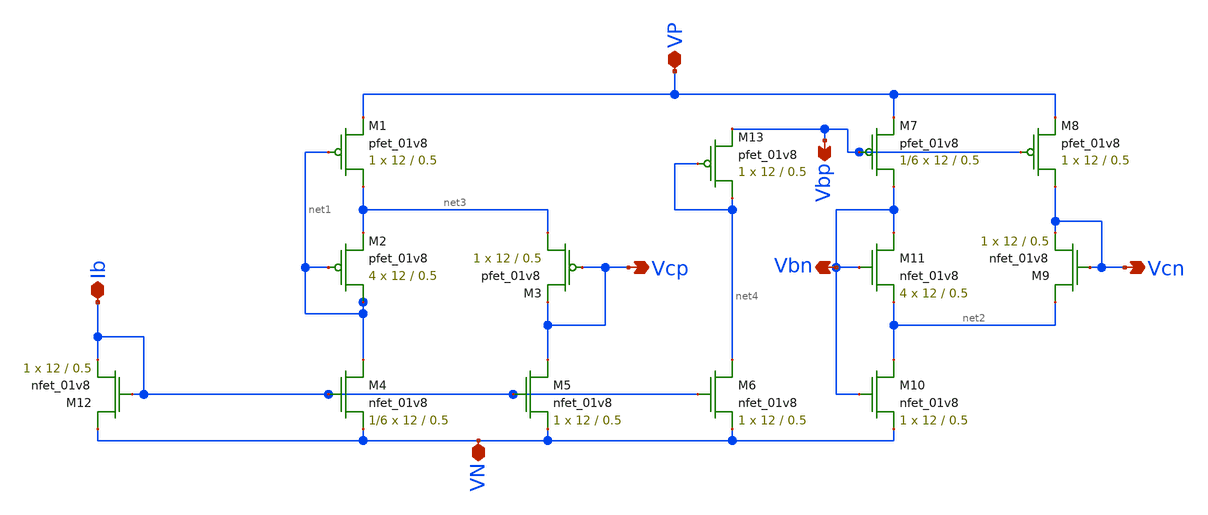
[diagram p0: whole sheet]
** sch_path: mp3/schematic/bias.sch
**.subckt bias VP VN Vcp Vcn Vbp Ib Vbn
*.iopin VP
*.iopin VN
*.opin Vcp
*.opin Vcn
*.opin Vbp
*.iopin Ib
*.opin Vbn
XM1 net3 net1 VP VDD sky130_fd_pr__pfet_01v8 L=0.5 W=12 nf=1 ad='int((nf+1)/2) * W/nf * 0.29' as='int((nf+2)/2) * W/nf * 0.29'
+ pd='2*int((nf+1)/2) * (W/nf + 0.29)' ps='2*int((nf+2)/2) * (W/nf + 0.29)' nrd='0.29 / W' nrs='0.29 / W'
+ sa=0 sb=0 sd=0 mult=1 m=1
XM2 net1 net1 net3 VDD sky130_fd_pr__pfet_01v8 L=0.5 W=12 nf=1 ad='int((nf+1)/2) * W/nf * 0.29' as='int((nf+2)/2) * W/nf * 0.29'
+ pd='2*int((nf+1)/2) * (W/nf + 0.29)' ps='2*int((nf+2)/2) * (W/nf + 0.29)' nrd='0.29 / W' nrs='0.29 / W'
+ sa=0 sb=0 sd=0 mult=4 m=4
XM3 net3 Vcp Vcp VDD sky130_fd_pr__pfet_01v8 L=0.5 W=12 nf=1 ad='int((nf+1)/2) * W/nf * 0.29' as='int((nf+2)/2) * W/nf * 0.29'
+ pd='2*int((nf+1)/2) * (W/nf + 0.29)' ps='2*int((nf+2)/2) * (W/nf + 0.29)' nrd='0.29 / W' nrs='0.29 / W'
+ sa=0 sb=0 sd=0 mult=1 m=1
XM4 net1 Ib VN GND sky130_fd_pr__nfet_01v8 L=0.5 W=12 nf=1 ad='int((nf+1)/2) * W/nf * 0.29' as='int((nf+2)/2) * W/nf * 0.29'
+ pd='2*int((nf+1)/2) * (W/nf + 0.29)' ps='2*int((nf+2)/2) * (W/nf + 0.29)' nrd='0.29 / W' nrs='0.29 / W'
+ sa=0 sb=0 sd=0 mult=1/6 m=1/6
XM5 Vcp Ib VN GND sky130_fd_pr__nfet_01v8 L=0.5 W=12 nf=1 ad='int((nf+1)/2) * W/nf * 0.29' as='int((nf+2)/2) * W/nf * 0.29'
+ pd='2*int((nf+1)/2) * (W/nf + 0.29)' ps='2*int((nf+2)/2) * (W/nf + 0.29)' nrd='0.29 / W' nrs='0.29 / W'
+ sa=0 sb=0 sd=0 mult=1 m=1
XM6 net4 Ib VN GND sky130_fd_pr__nfet_01v8 L=0.5 W=12 nf=1 ad='int((nf+1)/2) * W/nf * 0.29' as='int((nf+2)/2) * W/nf * 0.29'
+ pd='2*int((nf+1)/2) * (W/nf + 0.29)' ps='2*int((nf+2)/2) * (W/nf + 0.29)' nrd='0.29 / W' nrs='0.29 / W'
+ sa=0 sb=0 sd=0 mult=1 m=1
XM7 Vbn Vbp VP VDD sky130_fd_pr__pfet_01v8 L=0.5 W=12 nf=1 ad='int((nf+1)/2) * W/nf * 0.29' as='int((nf+2)/2) * W/nf * 0.29'
+ pd='2*int((nf+1)/2) * (W/nf + 0.29)' ps='2*int((nf+2)/2) * (W/nf + 0.29)' nrd='0.29 / W' nrs='0.29 / W'
+ sa=0 sb=0 sd=0 mult=1/6 m=1/6
XM8 Vcn Vbp VP VDD sky130_fd_pr__pfet_01v8 L=0.5 W=12 nf=1 ad='int((nf+1)/2) * W/nf * 0.29' as='int((nf+2)/2) * W/nf * 0.29'
+ pd='2*int((nf+1)/2) * (W/nf + 0.29)' ps='2*int((nf+2)/2) * (W/nf + 0.29)' nrd='0.29 / W' nrs='0.29 / W'
+ sa=0 sb=0 sd=0 mult=1 m=1
XM9 net2 Vcn Vcn GND sky130_fd_pr__nfet_01v8 L=0.5 W=12 nf=1 ad='int((nf+1)/2) * W/nf * 0.29' as='int((nf+2)/2) * W/nf * 0.29'
+ pd='2*int((nf+1)/2) * (W/nf + 0.29)' ps='2*int((nf+2)/2) * (W/nf + 0.29)' nrd='0.29 / W' nrs='0.29 / W'
+ sa=0 sb=0 sd=0 mult=1 m=1
XM10 net2 Vbn VN GND sky130_fd_pr__nfet_01v8 L=0.5 W=12 nf=1 ad='int((nf+1)/2) * W/nf * 0.29' as='int((nf+2)/2) * W/nf * 0.29'
+ pd='2*int((nf+1)/2) * (W/nf + 0.29)' ps='2*int((nf+2)/2) * (W/nf + 0.29)' nrd='0.29 / W' nrs='0.29 / W'
+ sa=0 sb=0 sd=0 mult=1 m=1
XM11 Vbn Vbn net2 GND sky130_fd_pr__nfet_01v8 L=0.5 W=12 nf=1 ad='int((nf+1)/2) * W/nf * 0.29' as='int((nf+2)/2) * W/nf * 0.29'
+ pd='2*int((nf+1)/2) * (W/nf + 0.29)' ps='2*int((nf+2)/2) * (W/nf + 0.29)' nrd='0.29 / W' nrs='0.29 / W'
+ sa=0 sb=0 sd=0 mult=4 m=4
XM12 VN Ib Ib GND sky130_fd_pr__nfet_01v8 L=0.5 W=12 nf=1 ad='int((nf+1)/2) * W/nf * 0.29' as='int((nf+2)/2) * W/nf * 0.29'
+ pd='2*int((nf+1)/2) * (W/nf + 0.29)' ps='2*int((nf+2)/2) * (W/nf + 0.29)' nrd='0.29 / W' nrs='0.29 / W'
+ sa=0 sb=0 sd=0 mult=1 m=1
XM13 net4 net4 Vbp VDD sky130_fd_pr__pfet_01v8 L=0.5 W=12 nf=1 ad='int((nf+1)/2) * W/nf * 0.29' as='int((nf+2)/2) * W/nf * 0.29'
+ pd='2*int((nf+1)/2) * (W/nf + 0.29)' ps='2*int((nf+2)/2) * (W/nf + 0.29)' nrd='0.29 / W' nrs='0.29 / W'
+ sa=0 sb=0 sd=0 mult=1 m=1
**.ends
.end
